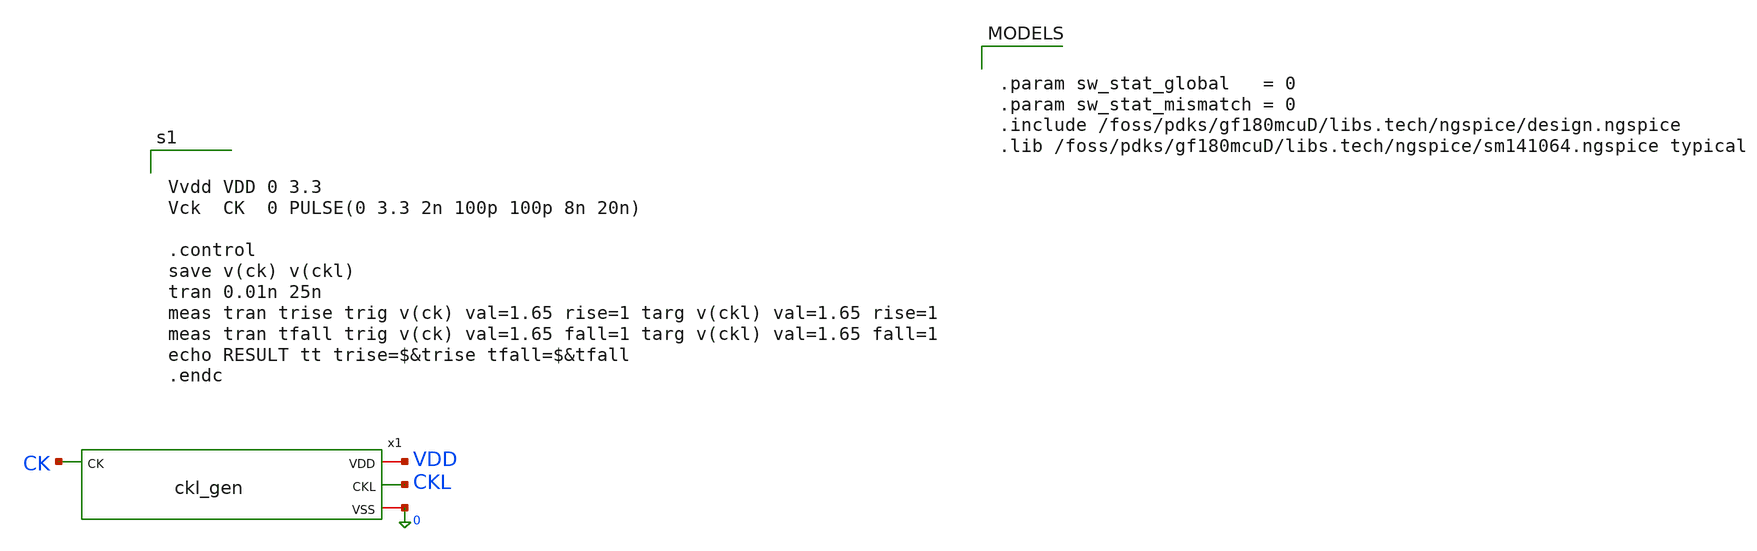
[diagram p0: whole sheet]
** sch_path: comparator_alt/schematic/tb_ckl_gen.sch
**.subckt tb_ckl_gen
x1 VDD CKL CK 0 ckl_gen
**** begin user architecture code


.param sw_stat_global   = 0
.param sw_stat_mismatch = 0
.include /foss/pdks/gf180mcuD/libs.tech/ngspice/design.ngspice
.lib /foss/pdks/gf180mcuD/libs.tech/ngspice/sm141064.ngspice typical




Vvdd VDD 0 3.3
Vck  CK  0 PULSE(0 3.3 2n 100p 100p 8n 20n)

.control
save v(ck) v(ckl)
tran 0.01n 25n
meas tran trise trig v(ck) val=1.65 rise=1 targ v(ckl) val=1.65 rise=1
meas tran tfall trig v(ck) val=1.65 fall=1 targ v(ckl) val=1.65 fall=1
echo RESULT tt trise=$&trise tfall=$&tfall
.endc


**** end user architecture code
**.ends

* expanding   symbol:  comparator_alt/schematic/ckl_gen.sym # of pins=4
** sym_path: comparator_alt/schematic/ckl_gen.sym
** sch_path: comparator_alt/schematic/ckl_gen.sch
.subckt ckl_gen VDD CKL CK VSS
*.iopin VDD
*.iopin VSS
*.ipin CK
*.opin CKL
x1 VDD net3 CK VSS inv_slow
x2 VDD net4 net3 VSS inv_slow
x3 VDD net5 net4 VSS inv_slow
x4 VDD net6 net5 VSS inv_slow
x5 VDD net7 net6 VSS inv_slow
x6 VDD CKD net7 VSS inv_slow
XM1 net1 CK VDD VDD pfet_03v3 L=0.28u W=2u nf=1 ad='int((nf+1)/2) * W/nf * 0.18u' as='int((nf+2)/2) * W/nf * 0.18u'
+ pd='2*int((nf+1)/2) * (W/nf + 0.18u)' ps='2*int((nf+2)/2) * (W/nf + 0.18u)' nrd='0.18u / W' nrs='0.18u / W'
+ sa=0 sb=0 sd=0 m=1
XM2 net1 CKD VDD VDD pfet_03v3 L=0.28u W=2u nf=1 ad='int((nf+1)/2) * W/nf * 0.18u' as='int((nf+2)/2) * W/nf * 0.18u'
+ pd='2*int((nf+1)/2) * (W/nf + 0.18u)' ps='2*int((nf+2)/2) * (W/nf + 0.18u)' nrd='0.18u / W' nrs='0.18u / W'
+ sa=0 sb=0 sd=0 m=1
XM3 net1 CK net2 VSS nfet_03v3 L=0.28u W=2u nf=1 ad='int((nf+1)/2) * W/nf * 0.18u' as='int((nf+2)/2) * W/nf * 0.18u'
+ pd='2*int((nf+1)/2) * (W/nf + 0.18u)' ps='2*int((nf+2)/2) * (W/nf + 0.18u)' nrd='0.18u / W' nrs='0.18u / W'
+ sa=0 sb=0 sd=0 m=1
XM4 net2 CKD VSS VSS nfet_03v3 L=0.28u W=2u nf=1 ad='int((nf+1)/2) * W/nf * 0.18u' as='int((nf+2)/2) * W/nf * 0.18u'
+ pd='2*int((nf+1)/2) * (W/nf + 0.18u)' ps='2*int((nf+2)/2) * (W/nf + 0.18u)' nrd='0.18u / W' nrs='0.18u / W'
+ sa=0 sb=0 sd=0 m=1
XM5 CKL net1 VSS VSS nfet_03v3 L=0.28u W=1u nf=1 ad='int((nf+1)/2) * W/nf * 0.18u' as='int((nf+2)/2) * W/nf * 0.18u'
+ pd='2*int((nf+1)/2) * (W/nf + 0.18u)' ps='2*int((nf+2)/2) * (W/nf + 0.18u)' nrd='0.18u / W' nrs='0.18u / W'
+ sa=0 sb=0 sd=0 m=1
XM6 CKL net1 VDD VDD pfet_03v3 L=0.28u W=2u nf=1 ad='int((nf+1)/2) * W/nf * 0.18u' as='int((nf+2)/2) * W/nf * 0.18u'
+ pd='2*int((nf+1)/2) * (W/nf + 0.18u)' ps='2*int((nf+2)/2) * (W/nf + 0.18u)' nrd='0.18u / W' nrs='0.18u / W'
+ sa=0 sb=0 sd=0 m=1
.ends


* expanding   symbol:  comparator_alt/schematic/inv_slow.sym # of pins=4
** sym_path: comparator_alt/schematic/inv_slow.sym
** sch_path: comparator_alt/schematic/inv_slow.sch
.subckt inv_slow VDD Y A VSS
*.iopin VDD
*.iopin VSS
*.opin Y
*.ipin A
XMT1 Y A VSS VSS nfet_03v3 L=1u W=1u nf=1 ad='int((nf+1)/2) * W/nf * 0.18u' as='int((nf+2)/2) * W/nf * 0.18u'
+ pd='2*int((nf+1)/2) * (W/nf + 0.18u)' ps='2*int((nf+2)/2) * (W/nf + 0.18u)' nrd='0.18u / W' nrs='0.18u / W'
+ sa=0 sb=0 sd=0 m=1
XM1 Y A VDD VDD pfet_03v3 L=1u W=2u nf=1 ad='int((nf+1)/2) * W/nf * 0.18u' as='int((nf+2)/2) * W/nf * 0.18u'
+ pd='2*int((nf+1)/2) * (W/nf + 0.18u)' ps='2*int((nf+2)/2) * (W/nf + 0.18u)' nrd='0.18u / W' nrs='0.18u / W'
+ sa=0 sb=0 sd=0 m=1
.ends

.end
